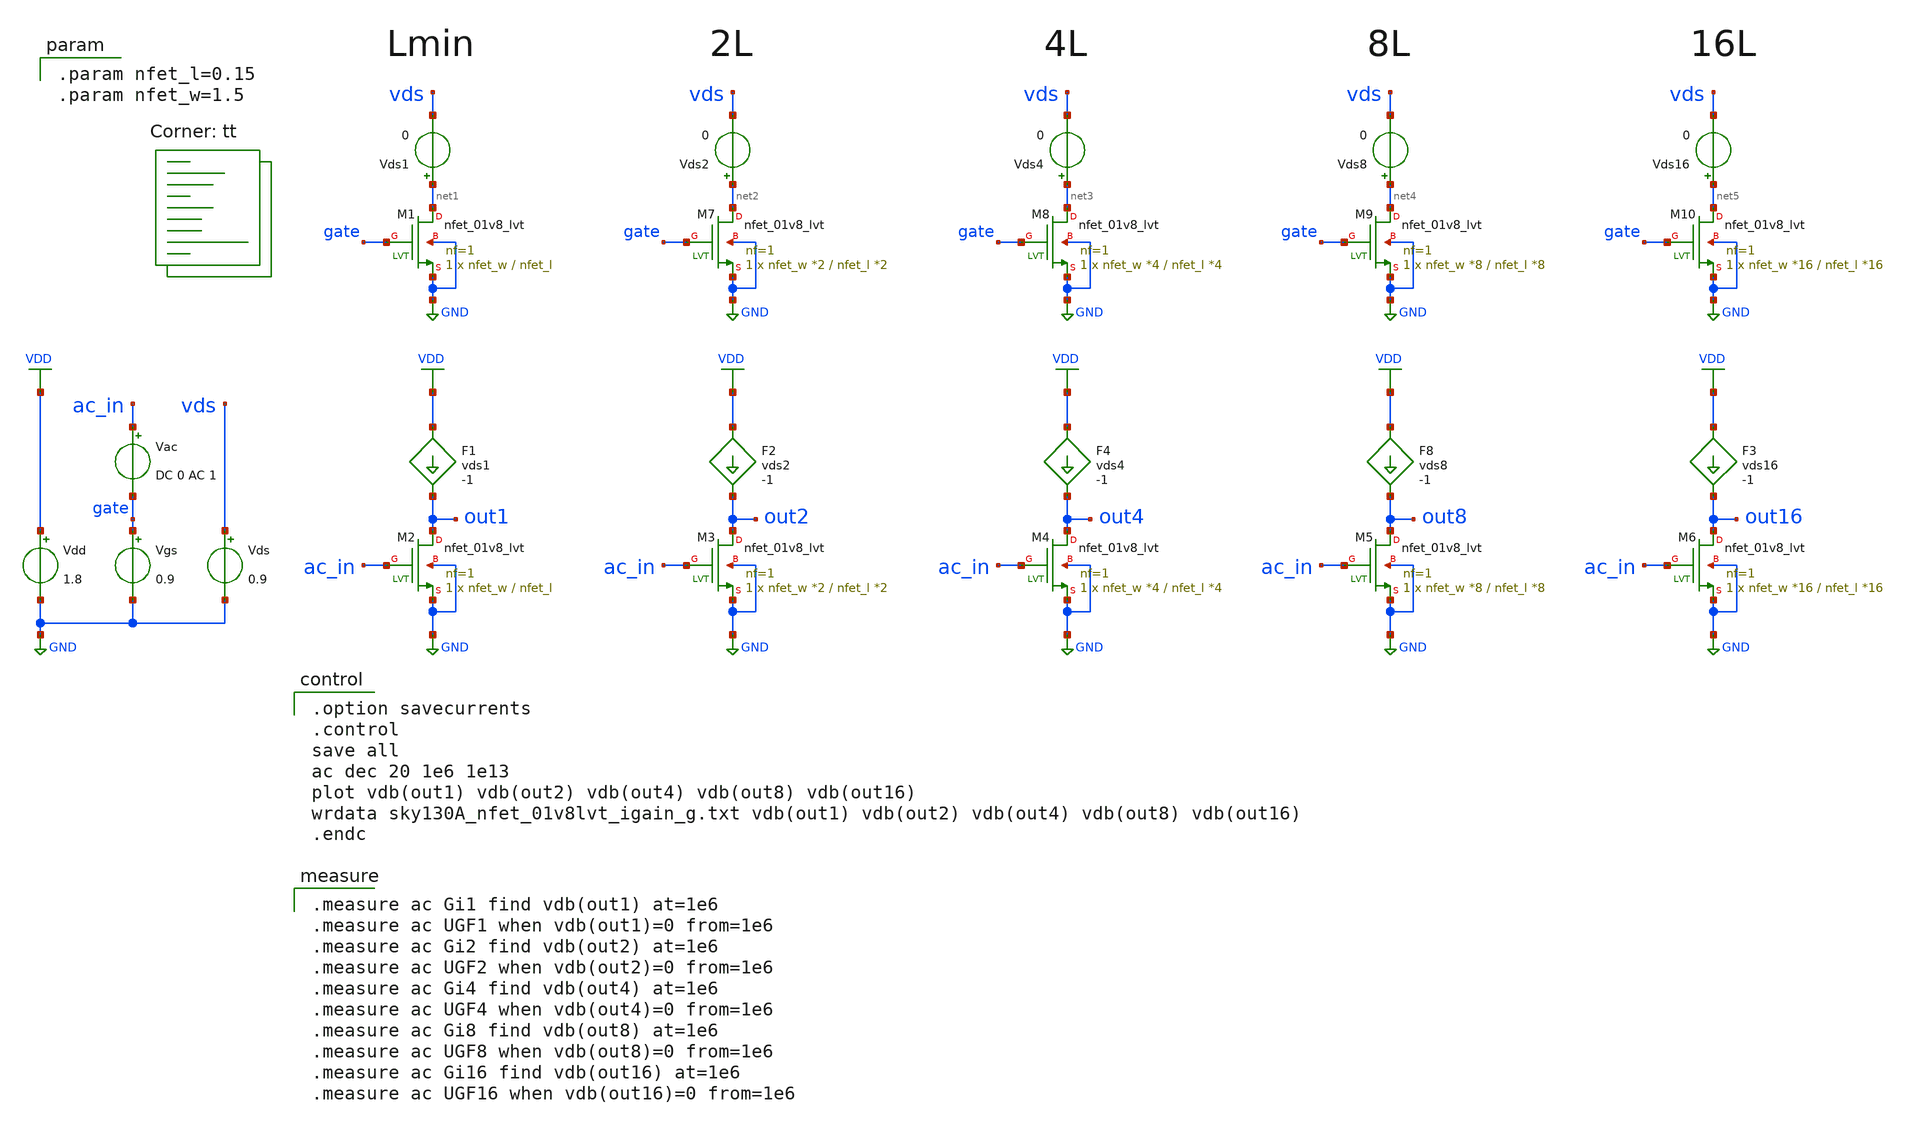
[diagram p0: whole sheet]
** sch_path: xschem/MOSFET/sky130A_nfet_01v8lvt_igain.sch
**.subckt sky130A_nfet_01v8lvt_igain
Vgs gate GND 0.9
Vdd VDD GND 1.8
F1 VDD out1 vds1 -1
Vds vds GND 0.9
Vac ac_in gate DC 0 AC 1
Vds1 net1 vds 0
F2 VDD out2 vds2 -1
Vds2 net2 vds 0
F4 VDD out4 vds4 -1
Vds4 net3 vds 0
F8 VDD out8 vds8 -1
Vds8 net4 vds 0
F3 VDD out16 vds16 -1
Vds16 net5 vds 0
XM1 net1 gate GND GND sky130_fd_pr__nfet_01v8_lvt L=nfet_l W=nfet_w nf=1 ad='int((1 + 1)/2) * nfet_w / 1 * 0.29'
+ as='int((1 + 2)/2) * nfet_w / 1 * 0.29' pd='2*int((1 + 1)/2) * (nfet_w / 1 + 0.29)' ps='2*int((1 + 2)/2) * (nfet_w / 1 + 0.29)'
+ nrd='0.29 / nfet_w ' nrs='0.29 / nfet_w ' sa=0 sb=0 sd=0 mult=1 m=1
XM2 out1 ac_in GND GND sky130_fd_pr__nfet_01v8_lvt L=nfet_l W=nfet_w nf=1 ad='int((1 + 1)/2) * nfet_w / 1 * 0.29'
+ as='int((1 + 2)/2) * nfet_w / 1 * 0.29' pd='2*int((1 + 1)/2) * (nfet_w / 1 + 0.29)' ps='2*int((1 + 2)/2) * (nfet_w / 1 + 0.29)'
+ nrd='0.29 / nfet_w ' nrs='0.29 / nfet_w ' sa=0 sb=0 sd=0 mult=1 m=1
XM3 out2 ac_in GND GND sky130_fd_pr__nfet_01v8_lvt L=nfet_l *2 W=nfet_w *2 nf=1 ad='int((1 + 1)/2) * nfet_w *2 / 1 * 0.29'
+ as='int((1 + 2)/2) * nfet_w *2 / 1 * 0.29' pd='2*int((1 + 1)/2) * (nfet_w *2 / 1 + 0.29)' ps='2*int((1 + 2)/2) * (nfet_w *2 / 1 + 0.29)'
+ nrd='0.29 / nfet_w *2 ' nrs='0.29 / nfet_w *2 ' sa=0 sb=0 sd=0 mult=1 m=1
XM4 out4 ac_in GND GND sky130_fd_pr__nfet_01v8_lvt L=nfet_l *4 W=nfet_w *4 nf=1 ad='int((1 + 1)/2) * nfet_w *4 / 1 * 0.29'
+ as='int((1 + 2)/2) * nfet_w *4 / 1 * 0.29' pd='2*int((1 + 1)/2) * (nfet_w *4 / 1 + 0.29)' ps='2*int((1 + 2)/2) * (nfet_w *4 / 1 + 0.29)'
+ nrd='0.29 / nfet_w *4 ' nrs='0.29 / nfet_w *4 ' sa=0 sb=0 sd=0 mult=1 m=1
XM5 out8 ac_in GND GND sky130_fd_pr__nfet_01v8_lvt L=nfet_l *8 W=nfet_w *8 nf=1 ad='int((1 + 1)/2) * nfet_w *8 / 1 * 0.29'
+ as='int((1 + 2)/2) * nfet_w *8 / 1 * 0.29' pd='2*int((1 + 1)/2) * (nfet_w *8 / 1 + 0.29)' ps='2*int((1 + 2)/2) * (nfet_w *8 / 1 + 0.29)'
+ nrd='0.29 / nfet_w *8 ' nrs='0.29 / nfet_w *8 ' sa=0 sb=0 sd=0 mult=1 m=1
XM6 out16 ac_in GND GND sky130_fd_pr__nfet_01v8_lvt L=nfet_l *16 W=nfet_w *16 nf=1 ad='int((1 + 1)/2) * nfet_w *16 / 1 * 0.29'
+ as='int((1 + 2)/2) * nfet_w *16 / 1 * 0.29' pd='2*int((1 + 1)/2) * (nfet_w *16 / 1 + 0.29)' ps='2*int((1 + 2)/2) * (nfet_w *16 / 1 + 0.29)'
+ nrd='0.29 / nfet_w *16 ' nrs='0.29 / nfet_w *16 ' sa=0 sb=0 sd=0 mult=1 m=1
XM7 net2 gate GND GND sky130_fd_pr__nfet_01v8_lvt L=nfet_l *2 W=nfet_w *2 nf=1 ad='int((1 + 1)/2) * nfet_w *2 / 1 * 0.29'
+ as='int((1 + 2)/2) * nfet_w *2 / 1 * 0.29' pd='2*int((1 + 1)/2) * (nfet_w *2 / 1 + 0.29)' ps='2*int((1 + 2)/2) * (nfet_w *2 / 1 + 0.29)'
+ nrd='0.29 / nfet_w *2 ' nrs='0.29 / nfet_w *2 ' sa=0 sb=0 sd=0 mult=1 m=1
XM8 net3 gate GND GND sky130_fd_pr__nfet_01v8_lvt L=nfet_l *4 W=nfet_w *4 nf=1 ad='int((1 + 1)/2) * nfet_w *4 / 1 * 0.29'
+ as='int((1 + 2)/2) * nfet_w *4 / 1 * 0.29' pd='2*int((1 + 1)/2) * (nfet_w *4 / 1 + 0.29)' ps='2*int((1 + 2)/2) * (nfet_w *4 / 1 + 0.29)'
+ nrd='0.29 / nfet_w *4 ' nrs='0.29 / nfet_w *4 ' sa=0 sb=0 sd=0 mult=1 m=1
XM9 net4 gate GND GND sky130_fd_pr__nfet_01v8_lvt L=nfet_l *8 W=nfet_w *8 nf=1 ad='int((1 + 1)/2) * nfet_w *8 / 1 * 0.29'
+ as='int((1 + 2)/2) * nfet_w *8 / 1 * 0.29' pd='2*int((1 + 1)/2) * (nfet_w *8 / 1 + 0.29)' ps='2*int((1 + 2)/2) * (nfet_w *8 / 1 + 0.29)'
+ nrd='0.29 / nfet_w *8 ' nrs='0.29 / nfet_w *8 ' sa=0 sb=0 sd=0 mult=1 m=1
XM10 net5 gate GND GND sky130_fd_pr__nfet_01v8_lvt L=nfet_l *16 W=nfet_w *16 nf=1 ad='int((1 + 1)/2) * nfet_w *16 / 1 * 0.29'
+ as='int((1 + 2)/2) * nfet_w *16 / 1 * 0.29' pd='2*int((1 + 1)/2) * (nfet_w *16 / 1 + 0.29)' ps='2*int((1 + 2)/2) * (nfet_w *16 / 1 + 0.29)'
+ nrd='0.29 / nfet_w *16 ' nrs='0.29 / nfet_w *16 ' sa=0 sb=0 sd=0 mult=1 m=1
**** begin user architecture code

.option savecurrents
.control
save all
ac dec 20 1e6 1e13
plot vdb(out1) vdb(out2) vdb(out4) vdb(out8) vdb(out16)
wrdata sky130A_nfet_01v8lvt_igain_g.txt vdb(out1) vdb(out2) vdb(out4) vdb(out8) vdb(out16)
.endc


.param nfet_l=0.15
.param nfet_w=1.5


.measure ac Gi1 find vdb(out1) at=1e6
.measure ac UGF1 when vdb(out1)=0 from=1e6
.measure ac Gi2 find vdb(out2) at=1e6
.measure ac UGF2 when vdb(out2)=0 from=1e6
.measure ac Gi4 find vdb(out4) at=1e6
.measure ac UGF4 when vdb(out4)=0 from=1e6
.measure ac Gi8 find vdb(out8) at=1e6
.measure ac UGF8 when vdb(out8)=0 from=1e6
.measure ac Gi16 find vdb(out16) at=1e6
.measure ac UGF16 when vdb(out16)=0 from=1e6

.lib $::SKYWATER_MODELS/sky130.lib.spice tt
**** end user architecture code
**.ends
.GLOBAL GND
.GLOBAL VDD
.end
